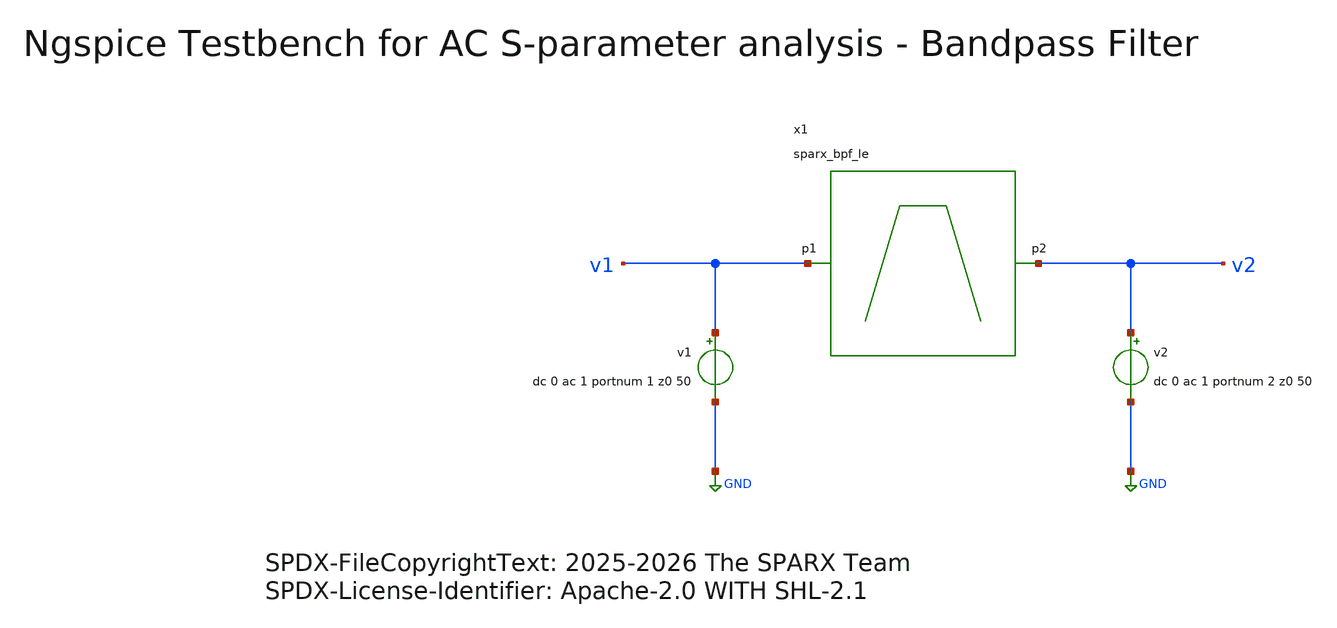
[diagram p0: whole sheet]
** sch_path: testbenches/xschem/sparx_bpf_le_tb_acsp_ngspice.sch
* SPDX-FileCopyrightText: 2025-2026 The SPARX Team
* SPDX-License-Identifier: Apache-2.0 WITH SHL-2.1
**.subckt sparx_bpf_le_tb_acsp_ngspice
v1 v1 GND dc 0 ac 1 portnum 1 z0 50
v2 v2 GND dc 0 ac 1 portnum 2 z0 50
x1 v1 v2 sparx_bpf_le
**** begin user architecture code


.include ../../../netlist/spice/sparx_bpf_le.spice
.include ../sim_range.spice
.param temp=27
.options savecurrents klu method=gear reltol=1e-3 abstol=1e-15 gmin=1e-15
.control

save all

set wr_vecnames
set wr_singlescale

* User Constants
* f_min / f_max come from ../sim_range.spice (.csparam),
* auto-synced to the loaded Touchstone by snp2le.
* edit that file for a standalone run.

* Operating Point Analysis
op
remzerovec
write @schname\.raw
set appendwrite

* AC S-Parameter Analysis
sp lin 1001 $&const.f_min $&const.f_max
remzerovec
write @schname\.raw
set appendwrite

* Calculating S-Parameters
let s11_dB = db(S_1_1)
let s21_dB = db(S_2_1)
let s12_dB = db(S_1_2)
let s22_dB = db(S_2_2)

let s11_deg = cph(S_1_1) * 180/pi
let s21_deg = cph(S_2_1) * 180/pi
let s12_deg = cph(S_1_2) * 180/pi
let s22_deg = cph(S_2_2) * 180/pi

* Plotting
plot s11_dB s22_dB
plot s11_deg s22_deg
plot s12_dB s21_dB
plot s12_deg s21_deg

* Write Data
unset appendwrite
set wr_vecnames
set wr_singlescale
wrdata ../plot_simulations/data/@schname\.txt  s11_dB s22_dB s12_dB s21_dB  s11_deg s22_deg s12_deg
+ s21_deg

*quit
.endc



.lib cornerMOSlv.lib mos_tt
.lib cornerMOShv.lib mos_tt
.lib cornerHBT.lib hbt_typ
.lib cornerRES.lib res_typ
.lib cornerCAP.lib cap_typ
.lib cornerDIO.lib dio_tt

**** end user architecture code
**.ends
.GLOBAL GND
.end
